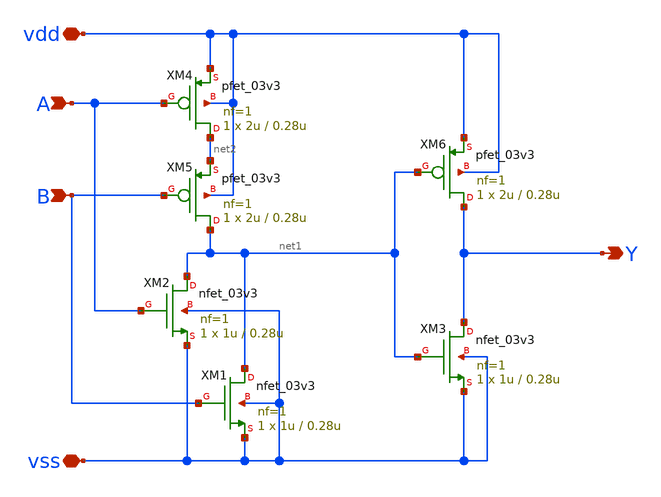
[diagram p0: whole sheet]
** sch_path: General/ADC/delay/or.sch
**.subckt or vdd vss A B Y
*.iopin vdd
*.iopin vss
*.ipin A
*.ipin B
*.opin Y
XM1 net1 B vss vss nfet_03v3 L=0.28u W=1u nf=1 ad='int((nf+1)/2) * W/nf * 0.18u' as='int((nf+2)/2) * W/nf * 0.18u'
+ pd='2*int((nf+1)/2) * (W/nf + 0.18u)' ps='2*int((nf+2)/2) * (W/nf + 0.18u)' nrd='0.18u / W' nrs='0.18u / W'
+ sa=0 sb=0 sd=0 m=1
XM2 net1 A vss vss nfet_03v3 L=0.28u W=1u nf=1 ad='int((nf+1)/2) * W/nf * 0.18u' as='int((nf+2)/2) * W/nf * 0.18u'
+ pd='2*int((nf+1)/2) * (W/nf + 0.18u)' ps='2*int((nf+2)/2) * (W/nf + 0.18u)' nrd='0.18u / W' nrs='0.18u / W'
+ sa=0 sb=0 sd=0 m=1
XM3 Y net1 vss vss nfet_03v3 L=0.28u W=1u nf=1 ad='int((nf+1)/2) * W/nf * 0.18u' as='int((nf+2)/2) * W/nf * 0.18u'
+ pd='2*int((nf+1)/2) * (W/nf + 0.18u)' ps='2*int((nf+2)/2) * (W/nf + 0.18u)' nrd='0.18u / W' nrs='0.18u / W'
+ sa=0 sb=0 sd=0 m=1
XM4 net2 A vdd vdd pfet_03v3 L=0.28u W=2u nf=1 ad='int((nf+1)/2) * W/nf * 0.18u' as='int((nf+2)/2) * W/nf * 0.18u'
+ pd='2*int((nf+1)/2) * (W/nf + 0.18u)' ps='2*int((nf+2)/2) * (W/nf + 0.18u)' nrd='0.18u / W' nrs='0.18u / W'
+ sa=0 sb=0 sd=0 m=1
XM5 net1 B net2 vdd pfet_03v3 L=0.28u W=2u nf=1 ad='int((nf+1)/2) * W/nf * 0.18u' as='int((nf+2)/2) * W/nf * 0.18u'
+ pd='2*int((nf+1)/2) * (W/nf + 0.18u)' ps='2*int((nf+2)/2) * (W/nf + 0.18u)' nrd='0.18u / W' nrs='0.18u / W'
+ sa=0 sb=0 sd=0 m=1
XM6 Y net1 vdd vdd pfet_03v3 L=0.28u W=2u nf=1 ad='int((nf+1)/2) * W/nf * 0.18u' as='int((nf+2)/2) * W/nf * 0.18u'
+ pd='2*int((nf+1)/2) * (W/nf + 0.18u)' ps='2*int((nf+2)/2) * (W/nf + 0.18u)' nrd='0.18u / W' nrs='0.18u / W'
+ sa=0 sb=0 sd=0 m=1
**.ends
.end
